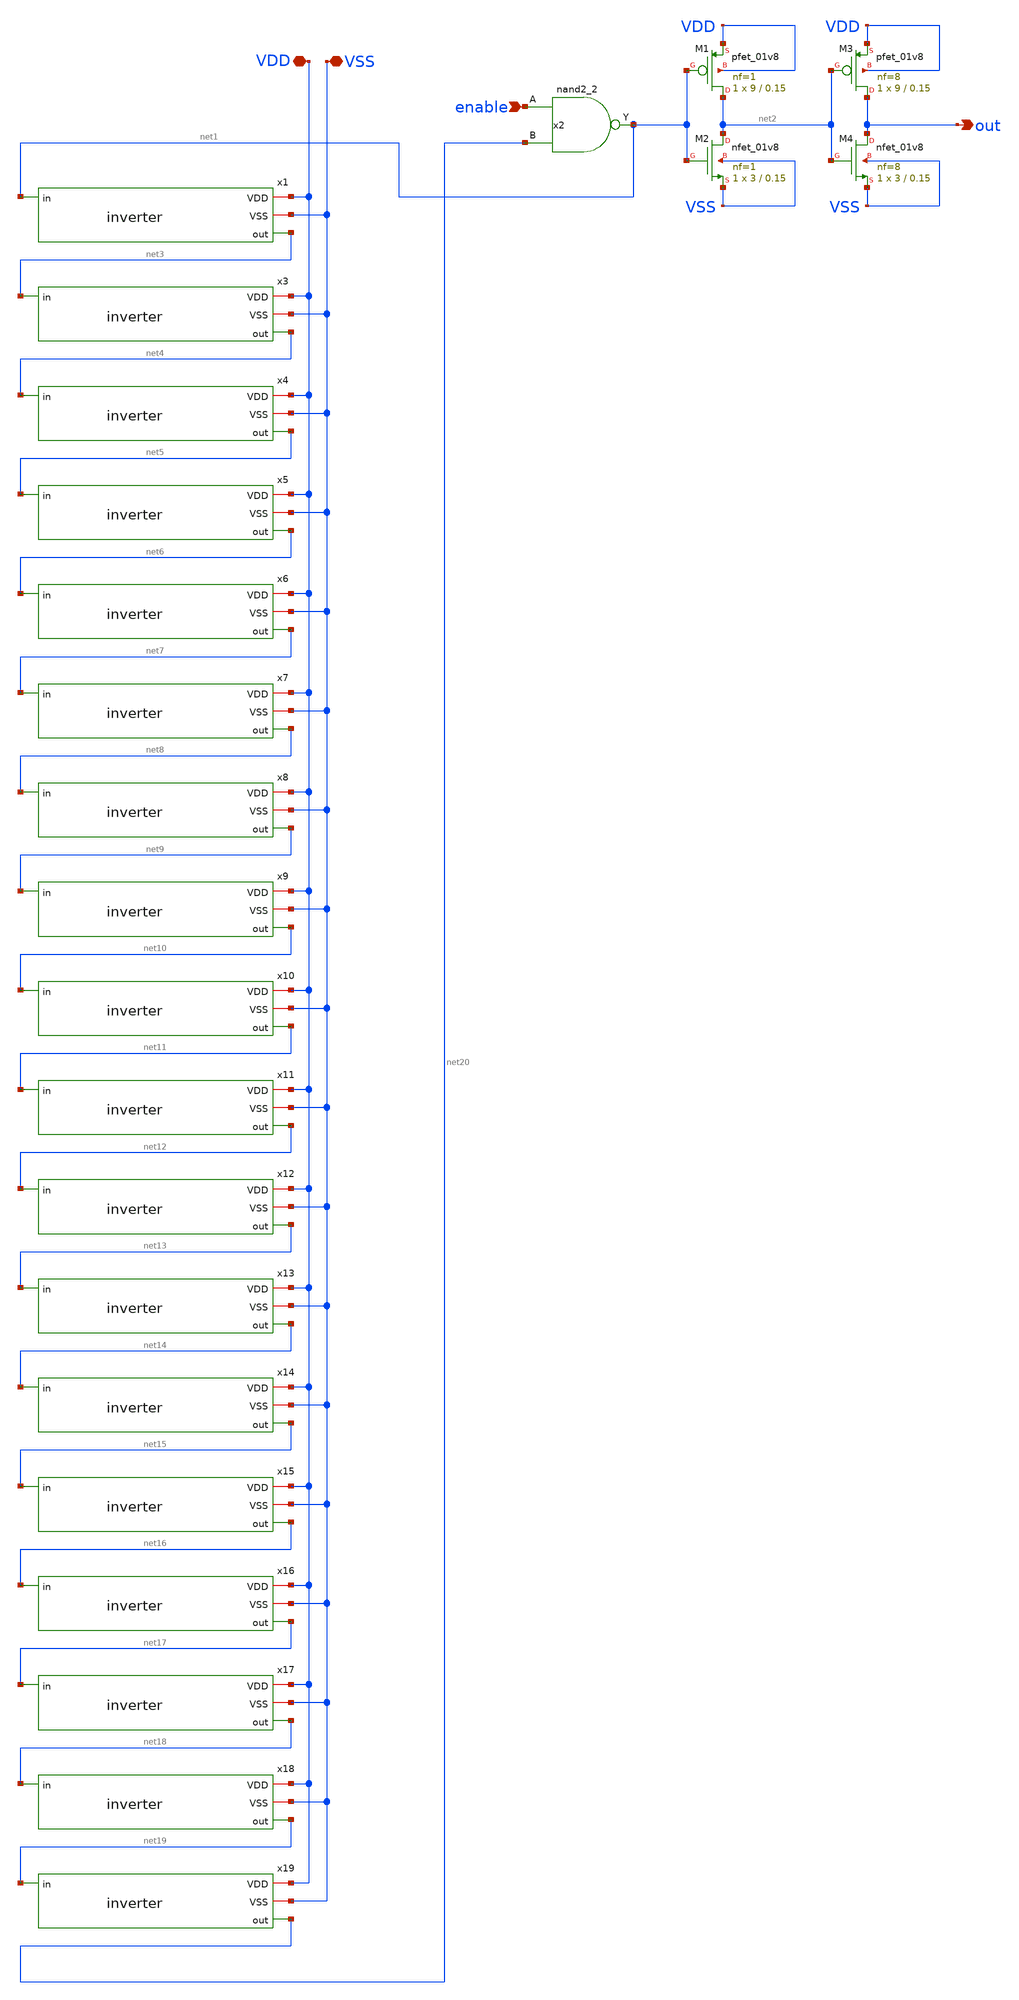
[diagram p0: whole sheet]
** sch_path: xschem/ring.sch
**.subckt ring VDD enable out VSS
*.iopin VDD
*.ipin enable
*.opin out
*.iopin VSS
x2 enable net20 VSS VSS VDD VDD net1 sky130_fd_sc_hd__nand2_2
XM1 net2 net1 VDD VDD sky130_fd_pr__pfet_01v8 L=0.15 W=9 nf=1 ad='int((nf+1)/2) * W/nf * 0.29' as='int((nf+2)/2) * W/nf * 0.29'
+ pd='2*int((nf+1)/2) * (W/nf + 0.29)' ps='2*int((nf+2)/2) * (W/nf + 0.29)' nrd='0.29 / W' nrs='0.29 / W'
+ sa=0 sb=0 sd=0 mult=1 m=1
XM2 net2 net1 VSS VSS sky130_fd_pr__nfet_01v8 L=0.15 W=3 nf=1 ad='int((nf+1)/2) * W/nf * 0.29' as='int((nf+2)/2) * W/nf * 0.29'
+ pd='2*int((nf+1)/2) * (W/nf + 0.29)' ps='2*int((nf+2)/2) * (W/nf + 0.29)' nrd='0.29 / W' nrs='0.29 / W'
+ sa=0 sb=0 sd=0 mult=1 m=1
x1 VDD VSS net1 net3 inverter
x3 VDD VSS net3 net4 inverter
x4 VDD VSS net4 net5 inverter
x5 VDD VSS net5 net6 inverter
x6 VDD VSS net6 net7 inverter
x7 VDD VSS net7 net8 inverter
x8 VDD VSS net8 net9 inverter
x9 VDD VSS net9 net10 inverter
x10 VDD VSS net10 net11 inverter
x11 VDD VSS net11 net12 inverter
x12 VDD VSS net12 net13 inverter
x13 VDD VSS net13 net14 inverter
x14 VDD VSS net14 net15 inverter
x15 VDD VSS net15 net16 inverter
x16 VDD VSS net16 net17 inverter
x17 VDD VSS net17 net18 inverter
x18 VDD VSS net18 net19 inverter
x19 VDD VSS net19 net20 inverter
XM3 out net2 VDD VDD sky130_fd_pr__pfet_01v8 L=0.15 W=9 nf=8 ad='int((nf+1)/2) * W/nf * 0.29' as='int((nf+2)/2) * W/nf * 0.29'
+ pd='2*int((nf+1)/2) * (W/nf + 0.29)' ps='2*int((nf+2)/2) * (W/nf + 0.29)' nrd='0.29 / W' nrs='0.29 / W'
+ sa=0 sb=0 sd=0 mult=1 m=1
XM4 out net2 VSS VSS sky130_fd_pr__nfet_01v8 L=0.15 W=3 nf=8 ad='int((nf+1)/2) * W/nf * 0.29' as='int((nf+2)/2) * W/nf * 0.29'
+ pd='2*int((nf+1)/2) * (W/nf + 0.29)' ps='2*int((nf+2)/2) * (W/nf + 0.29)' nrd='0.29 / W' nrs='0.29 / W'
+ sa=0 sb=0 sd=0 mult=1 m=1
**.ends

* expanding   symbol:  inverter.sym # of pins=4
** sym_path: xschem/inverter.sym
** sch_path: xschem/inverter.sch
.subckt inverter VDD VSS in out
*.opin out
*.iopin VDD
*.iopin VSS
*.ipin in
XM1 out in VDD VDD sky130_fd_pr__pfet_01v8 L=0.15 W=3 nf=1 ad='int((nf+1)/2) * W/nf * 0.29' as='int((nf+2)/2) * W/nf * 0.29'
+ pd='2*int((nf+1)/2) * (W/nf + 0.29)' ps='2*int((nf+2)/2) * (W/nf + 0.29)' nrd='0.29 / W' nrs='0.29 / W'
+ sa=0 sb=0 sd=0 mult=1 m=1
XM2 out in VSS VSS sky130_fd_pr__nfet_01v8 L=0.15 W=1 nf=1 ad='int((nf+1)/2) * W/nf * 0.29' as='int((nf+2)/2) * W/nf * 0.29'
+ pd='2*int((nf+1)/2) * (W/nf + 0.29)' ps='2*int((nf+2)/2) * (W/nf + 0.29)' nrd='0.29 / W' nrs='0.29 / W'
+ sa=0 sb=0 sd=0 mult=1 m=1
C6 in VSS 10fF m=1
.ends

.end
